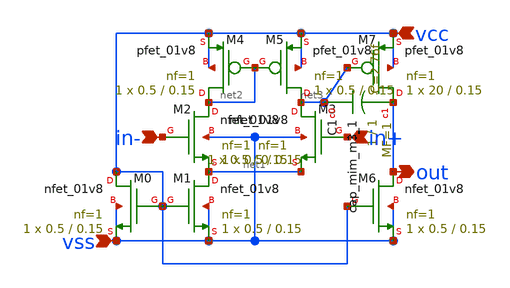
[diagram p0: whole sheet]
** sch_path: opamp.sch
**.subckt opamp out in- in+ vss vcc
*.opin out
*.ipin in-
*.ipin in+
*.ipin vss
*.ipin vcc
XM0 vcc vcc vss vss sky130_fd_pr__nfet_01v8 L=0.15 W=0.5 nf=1 ad='int((nf+1)/2) * W/nf * 0.29' as='int((nf+2)/2) * W/nf * 0.29'
+ pd='2*int((nf+1)/2) * (W/nf + 0.29)' ps='2*int((nf+2)/2) * (W/nf + 0.29)' nrd='0.29 / W' nrs='0.29 / W'
+ sa=0 sb=0 sd=0 mult=1 m=1
XM1 net1 vcc vss vss sky130_fd_pr__nfet_01v8 L=0.15 W=0.5 nf=1 ad='int((nf+1)/2) * W/nf * 0.29' as='int((nf+2)/2) * W/nf * 0.29'
+ pd='2*int((nf+1)/2) * (W/nf + 0.29)' ps='2*int((nf+2)/2) * (W/nf + 0.29)' nrd='0.29 / W' nrs='0.29 / W'
+ sa=0 sb=0 sd=0 mult=1 m=1
XM2 net2 in- net1 vss sky130_fd_pr__nfet_01v8 L=0.15 W=0.5 nf=1 ad='int((nf+1)/2) * W/nf * 0.29' as='int((nf+2)/2) * W/nf * 0.29'
+ pd='2*int((nf+1)/2) * (W/nf + 0.29)' ps='2*int((nf+2)/2) * (W/nf + 0.29)' nrd='0.29 / W' nrs='0.29 / W'
+ sa=0 sb=0 sd=0 mult=1 m=1
XM3 net3 in+ net1 vss sky130_fd_pr__nfet_01v8 L=0.15 W=0.5 nf=1 ad='int((nf+1)/2) * W/nf * 0.29' as='int((nf+2)/2) * W/nf * 0.29'
+ pd='2*int((nf+1)/2) * (W/nf + 0.29)' ps='2*int((nf+2)/2) * (W/nf + 0.29)' nrd='0.29 / W' nrs='0.29 / W'
+ sa=0 sb=0 sd=0 mult=1 m=1
XM4 net2 net2 vcc vcc sky130_fd_pr__pfet_01v8 L=0.15 W=0.5 nf=1 ad='int((nf+1)/2) * W/nf * 0.29' as='int((nf+2)/2) * W/nf * 0.29'
+ pd='2*int((nf+1)/2) * (W/nf + 0.29)' ps='2*int((nf+2)/2) * (W/nf + 0.29)' nrd='0.29 / W' nrs='0.29 / W'
+ sa=0 sb=0 sd=0 mult=1 m=1
XM5 net3 net2 vcc vcc sky130_fd_pr__pfet_01v8 L=0.15 W=0.5 nf=1 ad='int((nf+1)/2) * W/nf * 0.29' as='int((nf+2)/2) * W/nf * 0.29'
+ pd='2*int((nf+1)/2) * (W/nf + 0.29)' ps='2*int((nf+2)/2) * (W/nf + 0.29)' nrd='0.29 / W' nrs='0.29 / W'
+ sa=0 sb=0 sd=0 mult=1 m=1
XM7 out net3 vcc vcc sky130_fd_pr__pfet_01v8 L=0.15 W=20 nf=1 ad='int((nf+1)/2) * W/nf * 0.29' as='int((nf+2)/2) * W/nf * 0.29'
+ pd='2*int((nf+1)/2) * (W/nf + 0.29)' ps='2*int((nf+2)/2) * (W/nf + 0.29)' nrd='0.29 / W' nrs='0.29 / W'
+ sa=0 sb=0 sd=0 mult=1 m=1
XM6 out vcc vss vss sky130_fd_pr__nfet_01v8 L=0.15 W=0.5 nf=1 ad='int((nf+1)/2) * W/nf * 0.29' as='int((nf+2)/2) * W/nf * 0.29'
+ pd='2*int((nf+1)/2) * (W/nf + 0.29)' ps='2*int((nf+2)/2) * (W/nf + 0.29)' nrd='0.29 / W' nrs='0.29 / W'
+ sa=0 sb=0 sd=0 mult=1 m=1
XC1 net3 out sky130_fd_pr__cap_mim_m3_1 W=1 L=1 MF=1 m=1
**.ends
.end
